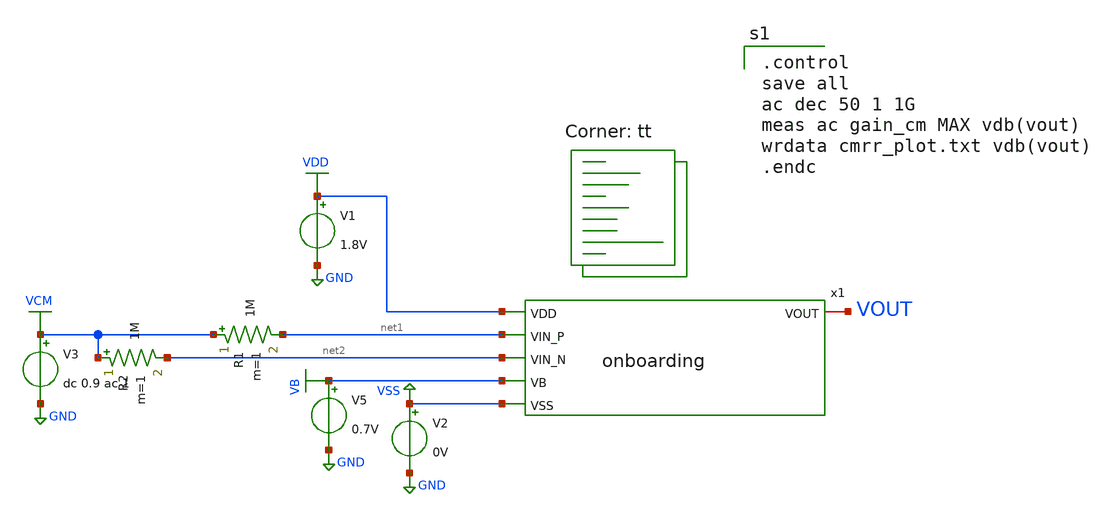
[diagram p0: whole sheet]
** sch_path: analog/bootcamp_opamp/build/schematic/tb_cmrr.sch
**.subckt tb_cmrr
V1 VDD GND 1.8V
V2 VSS GND 0V
V3 VCM GND dc 0.9 ac 1
R1 VCM net1 1M m=1
R2 VCM net2 1M m=1
V5 VB GND 0.7V
x1 VDD VOUT net1 net2 VB VSS onboarding
**** begin user architecture code
.lib $::SKYWATER_MODELS/sky130.lib.spice tt

.control
save all
ac dec 50 1 1G
meas ac gain_cm MAX vdb(vout)
wrdata cmrr_plot.txt vdb(vout)
.endc

**** end user architecture code
**.ends

* expanding   symbol:  onboarding.sym # of pins=6
** sym_path: analog/bootcamp_opamp/build/schematic/onboarding.sym
** sch_path: analog/bootcamp_opamp/build/schematic/onboarding.sch
.subckt onboarding VDD VOUT VIN_P VIN_N VB VSS
*.ipin VIN_P
*.ipin VDD
*.ipin VSS
*.ipin VB
*.ipin VIN_N
*.iopin VOUT
XC1 net4 VOUT sky130_fd_pr__cap_mim_m3_1 W=45 L=45 MF=1 m=1
XM6 VOUT net1 VDD VDD sky130_fd_pr__pfet_01v8 L=0.5 W=6 nf=1 ad='int((nf+1)/2) * W/nf * 0.29' as='int((nf+2)/2) * W/nf * 0.29'
+ pd='2*int((nf+1)/2) * (W/nf + 0.29)' ps='2*int((nf+2)/2) * (W/nf + 0.29)' nrd='0.29 / W' nrs='0.29 / W'
+ sa=0 sb=0 sd=0 mult=60 m=60
XM1 net3 VIN_P net2 VSS sky130_fd_pr__nfet_01v8 L=0.5 W=2 nf=1 ad='int((nf+1)/2) * W/nf * 0.29' as='int((nf+2)/2) * W/nf * 0.29'
+ pd='2*int((nf+1)/2) * (W/nf + 0.29)' ps='2*int((nf+2)/2) * (W/nf + 0.29)' nrd='0.29 / W' nrs='0.29 / W'
+ sa=0 sb=0 sd=0 mult=1 m=1
XM2 net1 VIN_N net2 VSS sky130_fd_pr__nfet_01v8 L=0.5 W=2 nf=1 ad='int((nf+1)/2) * W/nf * 0.29' as='int((nf+2)/2) * W/nf * 0.29'
+ pd='2*int((nf+1)/2) * (W/nf + 0.29)' ps='2*int((nf+2)/2) * (W/nf + 0.29)' nrd='0.29 / W' nrs='0.29 / W'
+ sa=0 sb=0 sd=0 mult=1 m=1
XM4 net1 net3 VDD VDD sky130_fd_pr__pfet_01v8 L=0.5 W=6 nf=1 ad='int((nf+1)/2) * W/nf * 0.29' as='int((nf+2)/2) * W/nf * 0.29'
+ pd='2*int((nf+1)/2) * (W/nf + 0.29)' ps='2*int((nf+2)/2) * (W/nf + 0.29)' nrd='0.29 / W' nrs='0.29 / W'
+ sa=0 sb=0 sd=0 mult=1 m=1
XM3 net3 net3 VDD VDD sky130_fd_pr__pfet_01v8 L=0.5 W=6 nf=1 ad='int((nf+1)/2) * W/nf * 0.29' as='int((nf+2)/2) * W/nf * 0.29'
+ pd='2*int((nf+1)/2) * (W/nf + 0.29)' ps='2*int((nf+2)/2) * (W/nf + 0.29)' nrd='0.29 / W' nrs='0.29 / W'
+ sa=0 sb=0 sd=0 mult=1 m=1
XM5 net2 VB VSS VSS sky130_fd_pr__nfet_01v8 L=0.5 W=2 nf=1 ad='int((nf+1)/2) * W/nf * 0.29' as='int((nf+2)/2) * W/nf * 0.29'
+ pd='2*int((nf+1)/2) * (W/nf + 0.29)' ps='2*int((nf+2)/2) * (W/nf + 0.29)' nrd='0.29 / W' nrs='0.29 / W'
+ sa=0 sb=0 sd=0 mult=1 m=1
XM7 VOUT VB VSS VSS sky130_fd_pr__nfet_01v8 L=0.5 W=4.6 nf=1 ad='int((nf+1)/2) * W/nf * 0.29' as='int((nf+2)/2) * W/nf * 0.29'
+ pd='2*int((nf+1)/2) * (W/nf + 0.29)' ps='2*int((nf+2)/2) * (W/nf + 0.29)' nrd='0.29 / W' nrs='0.29 / W'
+ sa=0 sb=0 sd=0 mult=10 m=10
XR1 net4 net1 sky130_fd_pr__res_generic_po W=1 L=5 m=1
.ends

.GLOBAL VDD
.GLOBAL GND
.GLOBAL VSS
.GLOBAL VCM
.GLOBAL VB
.end
